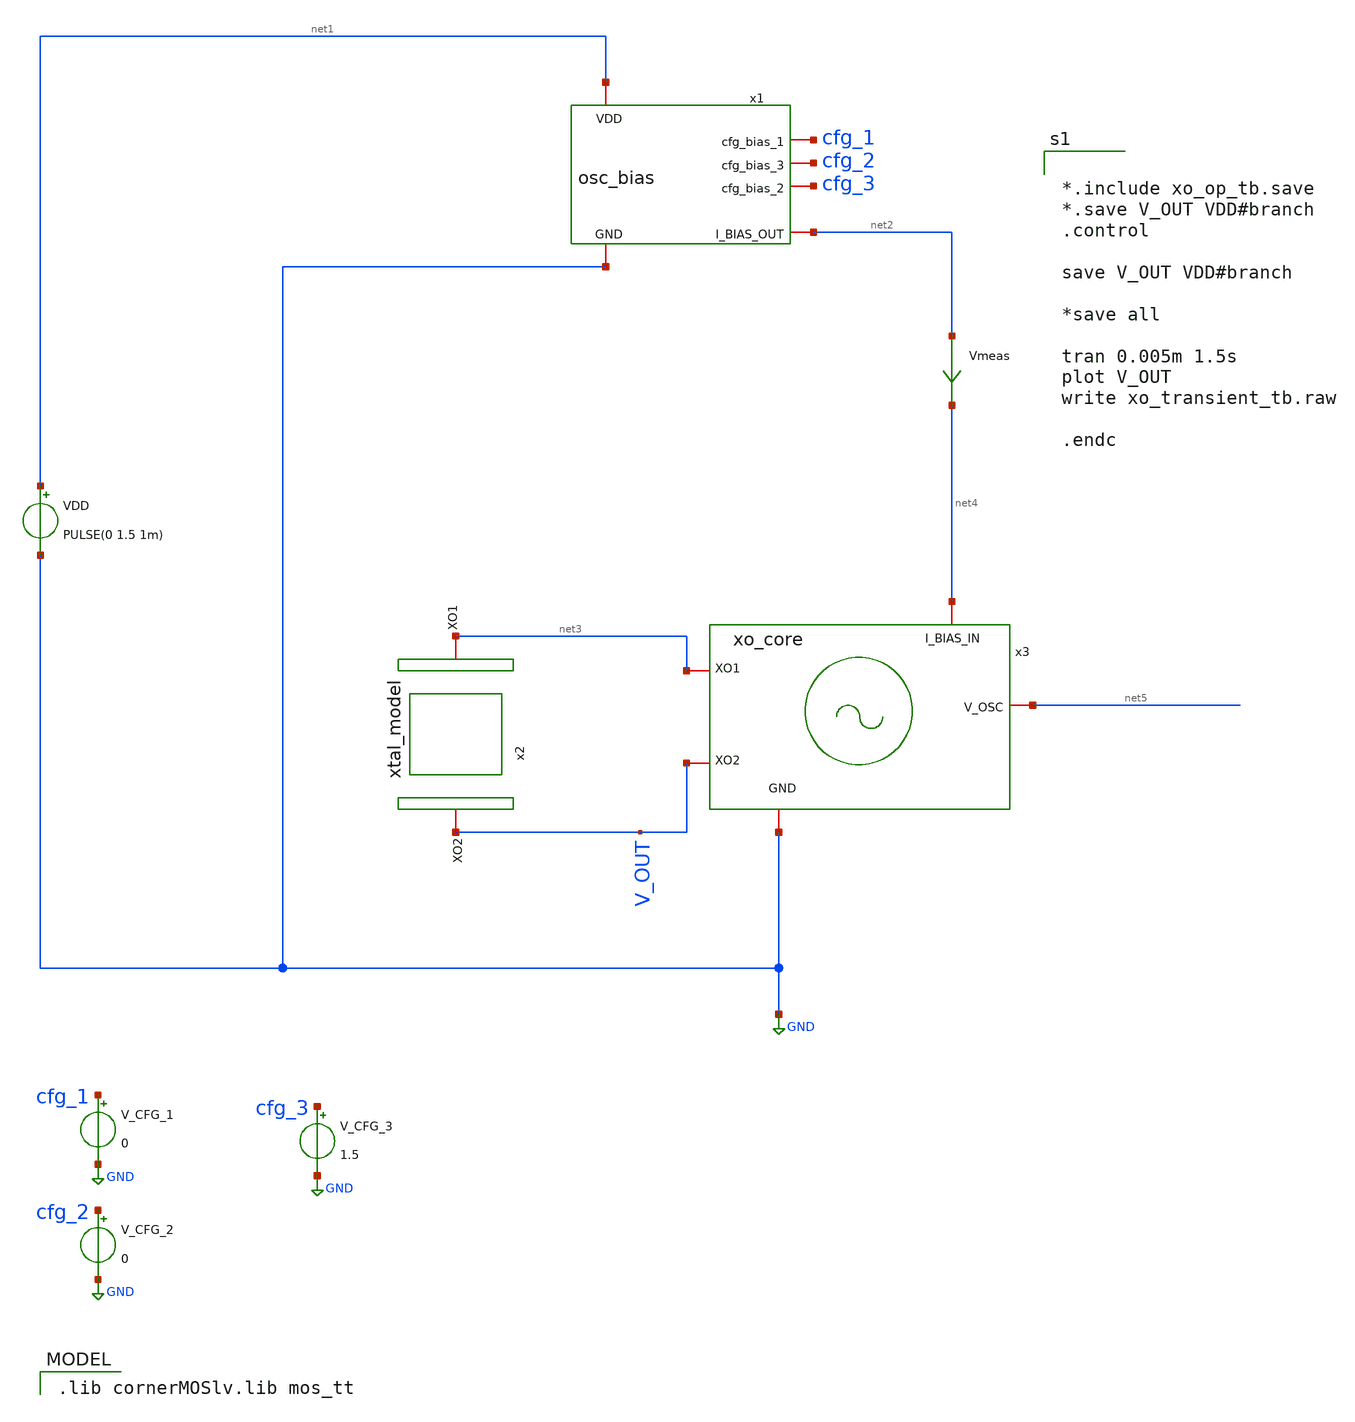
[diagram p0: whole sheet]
** sch_path: xo_transient_tb.sch
**.subckt xo_transient_tb
VDD net1 GND PULSE(0 1.5 1m)
x1 net1 cfg_1 cfg_2 cfg_3 GND net2 osc_bias
x2 net3 V_OUT xtal_model
x3 net4 net5 V_OUT net3 GND xo_core
V_CFG_1 cfg_1 GND 0
V_CFG_2 cfg_2 GND 0
V_CFG_3 cfg_3 GND 1.5
Vmeas net2 net4 0
.save i(vmeas)
**** begin user architecture code


*.include xo_op_tb.save
*.save V_OUT VDD#branch
.control

save V_OUT VDD#branch

*save all

tran 0.005m 1.5s
plot V_OUT
write xo_transient_tb.raw

.endc


 .lib cornerMOSlv.lib mos_tt

**** end user architecture code
**.ends

* expanding   symbol:  osc_bias.sym # of pins=6
** sym_path: osc_bias.sym
** sch_path: osc_bias.sch
.subckt osc_bias VDD cfg_bias_1 cfg_bias_3 cfg_bias_2 GND I_BIAS_OUT
*.iopin VDD
*.iopin GND
*.iopin I_BIAS_OUT
*.iopin cfg_bias_1
*.iopin cfg_bias_2
*.iopin cfg_bias_3
XM1 vp_bias vp_bias VDD VDD sg13_lv_pmos w=1u l=10u ng=1 m=1 mm_ok=1
XM3 vp_bias vp_bias net2 net1 sg13_lv_nmos w=0.25u l=10u ng=1 m=1 mm_ok=1
XM4 net2 net2 net3 net1 sg13_lv_nmos w=0.25u l=10u ng=1 m=1 mm_ok=1
XM5 net3 net3 net1 net1 sg13_lv_nmos w=0.25u l=10u ng=1 m=1 mm_ok=1
XM2 net7 vp_bias VDD VDD sg13_lv_pmos w=0.5u l=10u ng=1 m=1 mm_ok=1
XM6 I_BIAS_OUT cfg_bias_1 net7 VDD sg13_lv_pmos w=0.5u l=5u ng=1 m=1 mm_ok=1
XM7 net4 vp_bias VDD VDD sg13_lv_pmos w=0.5u l=10u ng=1 m=1 mm_ok=1
XM8 net5 vp_bias VDD VDD sg13_lv_pmos w=0.5u l=10u ng=1 m=1 mm_ok=1
XM9 I_BIAS_OUT cfg_bias_2 net4 VDD sg13_lv_pmos w=0.5u l=10u ng=1 m=1 mm_ok=1
XM10 I_BIAS_OUT cfg_bias_3 net5 VDD sg13_lv_pmos w=0.5u l=10u ng=1 m=1 mm_ok=1
XM11 net1 net1 net6 net1 sg13_lv_nmos w=0.25u l=10u ng=1 m=1 mm_ok=1
Vmeas net6 GND 0
.save i(vmeas)
.ends


* expanding   symbol:  xtal_model.sym # of pins=2
** sym_path: xtal_model.sym
** sch_path: xtal_model.sch
.subckt xtal_model XO1 XO2
*.iopin XO2
*.iopin XO1
R1 XO1 net1 1k m=1
Cm net1 net2 1p m=1
C0 XO1 XO2 1p m=1
Lm net2 XO2 1n m=1
.ends


* expanding   symbol:  xo_core.sym # of pins=5
** sym_path: xo_core.sym
** sch_path: xo_core.sch
.subckt xo_core I_BIAS_IN V_OSC XO2 XO1 GND
*.iopin GND
*.ipin XO2
*.ipin XO1
*.ipin I_BIAS_IN
*.opin V_OSC
XM2 net1 XO1 XO1 XO1 sg13_lv_pmos w=2u l=2u ng=1 m=1 mm_ok=1
XM3 XO2 net1 net1 net1 sg13_lv_pmos w=2u l=2u ng=1 m=1 mm_ok=1
XM1 XO2 XO1 GND GND sg13_lv_nmos w=0.5u l=1.0u ng=1 m=1 mm_ok=1
C2 XO2 GND 8p m=1
C1 XO1 GND 8p m=1
Vmeas I_BIAS_IN XO2 0
.save i(vmeas)
.ends

.GLOBAL GND
.end
